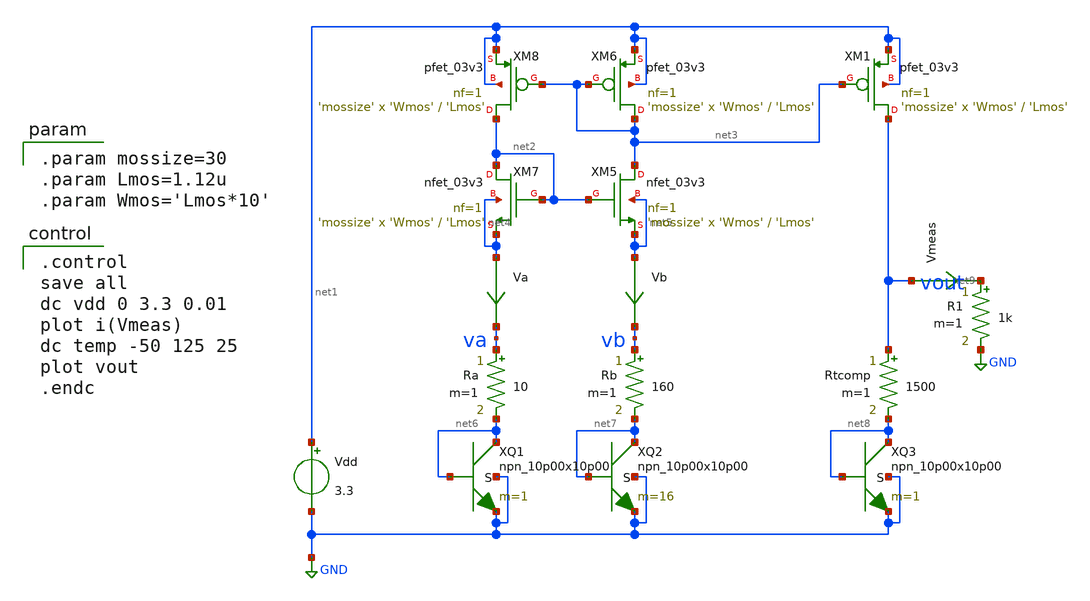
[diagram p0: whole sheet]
** sch_path: designs/First cut design/bgr-diode-currentmirror-tcomp.sch
**.subckt bgr-diode-currentmirror-tcomp
Vdd net1 GND 3.3
XM5 net3 net2 net5 net5 nfet_03v3 L='Lmos' W='Wmos' nf=1 ad='int((nf+1)/2) * W/nf * 0.18u' as='int((nf+2)/2) * W/nf * 0.18u'
+ pd='2*int((nf+1)/2) * (W/nf + 0.18u)' ps='2*int((nf+2)/2) * (W/nf + 0.18u)' nrd='0.18u / W' nrs='0.18u / W'
+ sa=0 sb=0 sd=0 m='mossize'
XM6 net3 net3 net1 net1 pfet_03v3 L='Lmos' W='Wmos' nf=1 ad='int((nf+1)/2) * W/nf * 0.18u' as='int((nf+2)/2) * W/nf * 0.18u'
+ pd='2*int((nf+1)/2) * (W/nf + 0.18u)' ps='2*int((nf+2)/2) * (W/nf + 0.18u)' nrd='0.18u / W' nrs='0.18u / W'
+ sa=0 sb=0 sd=0 m='mossize'
XM7 net2 net2 net4 net4 nfet_03v3 L='Lmos' W='Wmos' nf=1 ad='int((nf+1)/2) * W/nf * 0.18u' as='int((nf+2)/2) * W/nf * 0.18u'
+ pd='2*int((nf+1)/2) * (W/nf + 0.18u)' ps='2*int((nf+2)/2) * (W/nf + 0.18u)' nrd='0.18u / W' nrs='0.18u / W'
+ sa=0 sb=0 sd=0 m='mossize'
XM8 net2 net3 net1 net1 pfet_03v3 L='Lmos' W='Wmos' nf=1 ad='int((nf+1)/2) * W/nf * 0.18u' as='int((nf+2)/2) * W/nf * 0.18u'
+ pd='2*int((nf+1)/2) * (W/nf + 0.18u)' ps='2*int((nf+2)/2) * (W/nf + 0.18u)' nrd='0.18u / W' nrs='0.18u / W'
+ sa=0 sb=0 sd=0 m='mossize'
Vb net5 vb 0
.save i(vb)
Va net4 va 0
.save i(va)
XQ1 net6 net6 GND GND npn_10p00x10p00 m=1
XQ2 net7 net7 GND GND npn_10p00x10p00 m=16
Rb vb net7 160 m=1
Ra va net6 10 m=1
XM1 vout net3 net1 net1 pfet_03v3 L='Lmos' W='Wmos' nf=1 ad='int((nf+1)/2) * W/nf * 0.18u' as='int((nf+2)/2) * W/nf * 0.18u'
+ pd='2*int((nf+1)/2) * (W/nf + 0.18u)' ps='2*int((nf+2)/2) * (W/nf + 0.18u)' nrd='0.18u / W' nrs='0.18u / W'
+ sa=0 sb=0 sd=0 m='mossize'
XQ3 net8 net8 GND GND npn_10p00x10p00 m=1
Rtcomp vout net8 1500 m=1
Vmeas vout net9 0
.save i(vmeas)
R1 net9 GND 1k m=1
**** begin user architecture code

.include $::180MCU_MODELS/design.ngspice
.lib $::180MCU_MODELS/sm141064.ngspice typical
.lib $::180MCU_MODELS/sm141064.ngspice res_typical
.lib $::180MCU_MODELS/sm141064.ngspice moscap_typical
.lib $::180MCU_MODELS/sm141064.ngspice bjt_typical
* .lib $::180MCU_MODELS/sm141064.ngspice res_statistical


.control
save all
dc vdd 0 3.3 0.01
plot i(Vmeas)
dc temp -50 125 25
plot vout
.endc


.param mossize=30
.param Lmos=1.12u
.param Wmos='Lmos*10'

**** end user architecture code
**.ends
.GLOBAL GND
.end
